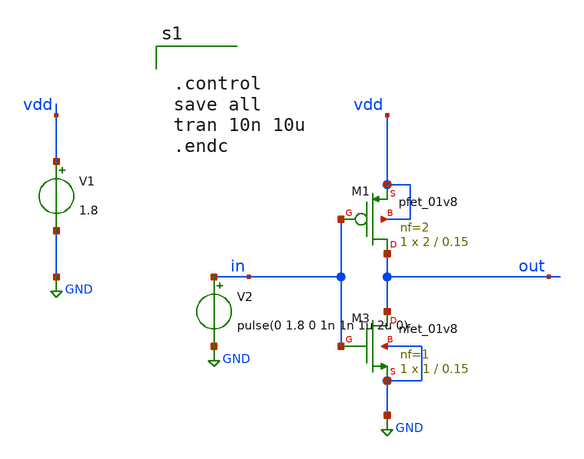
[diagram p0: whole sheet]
** sch_path: xschem/src/inverter/inverter_tb.sch
**.subckt inverter_tb
V1 vdd GND 1.8
V2 in GND pulse(0 1.8 0 1n 1n 1u 2u 0)
XM3 out in GND GND sky130_fd_pr__nfet_01v8 L=0.15 W=1 nf=1 ad='int((nf+1)/2) * W/nf * 0.29' as='int((nf+2)/2) * W/nf * 0.29'
+ pd='2*int((nf+1)/2) * (W/nf + 0.29)' ps='2*int((nf+2)/2) * (W/nf + 0.29)' nrd='0.29 / W' nrs='0.29 / W'
+ sa=0 sb=0 sd=0 mult=1 m=1
XM1 out in vdd vdd sky130_fd_pr__pfet_01v8 L=0.15 W=2 nf=2 ad='int((nf+1)/2) * W/nf * 0.29' as='int((nf+2)/2) * W/nf * 0.29'
+ pd='2*int((nf+1)/2) * (W/nf + 0.29)' ps='2*int((nf+2)/2) * (W/nf + 0.29)' nrd='0.29 / W' nrs='0.29 / W'
+ sa=0 sb=0 sd=0 mult=1 m=1
**** begin user architecture code

.include /home/eda/pdk/skywater-pdk/libraries/sky130_fd_pr_ngspice/latest/models/corners/tt.spice


* Resistor$::SKYWATER_MODELS/Capacitor
.include $::SKYWATER_MODELS/models/r+c/res_typical__cap_typical.spice
.include $::SKYWATER_MODELS/models/r+c/res_typical__cap_typical__lin.spice
* Special cells
.include $::SKYWATER_MODELS/models/corners/tt/specialized_cells.spice




.control
save all
tran 10n 10u
.endc



**** end user architecture code
**.ends
.GLOBAL GND
.end
